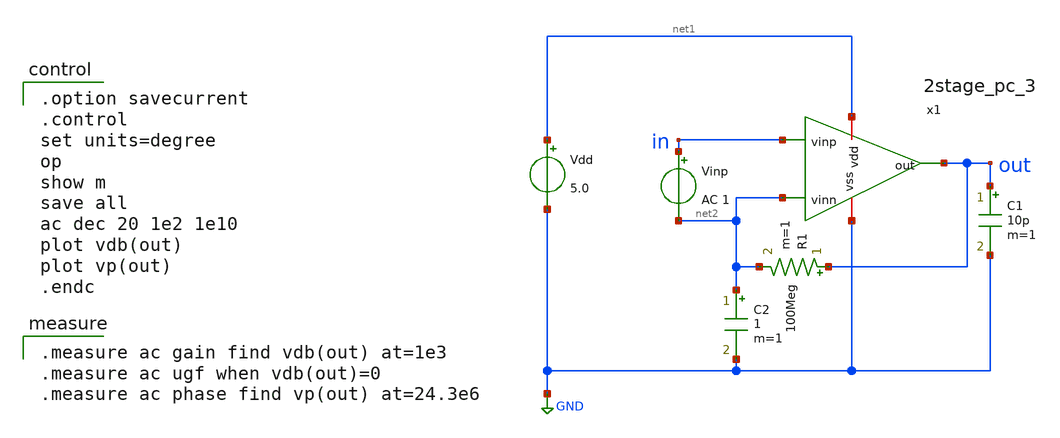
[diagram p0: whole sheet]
** sch_path: member_project/GroupWork/Team_Ando/ugeugeHigh/opamp_cs_ac.sch
**.subckt opamp_cs_ac
Vdd net1 GND 5.0
Vinp in net2 AC 1
C1 out GND 10p m=1
R1 out net2 100Meg m=1
C2 net2 GND 1 m=1
x1 net1 in out net2 GND 2stage_pc_3
**** begin user architecture code

.option savecurrent
.control
set units=degree
op
show m
save all
ac dec 20 1e2 1e10
plot vdb(out)
plot vp(out)
.endc


.measure ac gain find vdb(out) at=1e3
.measure ac ugf when vdb(out)=0
.measure ac phase find vp(out) at=24.3e6

 .include $::LIB/mos.lib
.include $::LIB/passive.lib
.include $::LIB/diode.lib
**** end user architecture code
**.ends

* expanding   symbol:  ishi/2stage_pc_3.sym # of pins=5
** sym_path: member_project/GroupWork/Team_Ando/ugeugeHigh/2stage_pc_3.sym
** sch_path: member_project/GroupWork/Team_Ando/ugeugeHigh/2stage_pc_3.sch
.subckt 2stage_pc_3 vdd vinp out vinn vss
*.ipin vinp
*.ipin vinn
*.opin out
*.iopin vdd
*.iopin vss
M2 net5 net2 net4 vss nmos L=2u W=40u m=1
M6 net2 net3 vdd vdd pmos L=2.5u W=10u m=1
M1 net2 net2 net1 vss nmos L=2u W=10u m=1
M7 net1 net1 vss vss nmos L=2u W=10u m=1
C1 out net5 poly_cap W=18 L=18
M3 net3 net3 vdd vdd pmos L=2.5u W=10u m=1
x1 vdd net3 vinn vinp net4 vss diffwl500-4
x2 vdd net3 out net4 vss source_g
M4 net3 net6 vss vss nmos L=2u W=5u m=1
M5 net6 net6 vss vss nmos L=2u W=5u m=1
M8 net6 net7 vdd vdd pmos L=2.5u W=10u m=1
x3 vdd net8 vss net7 VthRef
.ends


* expanding   symbol:  ishi/diffwl500-4.sym # of pins=6
** sym_path: member_project/GroupWork/Team_Ando/ugeugeHigh/diffwl500-4.sym
** sch_path: member_project/GroupWork/Team_Ando/ugeugeHigh/diffwl500-4.sch
.subckt diffwl500-4 vdd vb vinn vinp out VSS
*.ipin vinn
*.ipin vinp
*.iopin VSS
*.iopin vdd
*.ipin vb
*.opin out
M5 net1 vb vdd vdd pmos L=2u W=40u m=1
M3 net2 net2 VSS VSS nmos L=2u W=10u m=1
M1 net2 vinn net1 net1 pmos L=2u W=200u m=1
M2 out vinp net1 net1 pmos L=2u W=200u m=1
M4 out net2 VSS VSS nmos L=2u W=10u m=1
.ends


* expanding   symbol:  ishi/source_g.sym # of pins=5
** sym_path: member_project/GroupWork/Team_Ando/ugeugeHigh/source_g.sym
** sch_path: member_project/GroupWork/Team_Ando/ugeugeHigh/source_g.sch
.subckt source_g vdd vb out vin VSS
*.iopin vdd
*.opin out
*.ipin vb
*.ipin vin
*.iopin VSS
M2 out vin VSS VSS nmos L=2u W=200u m=1
M1 out vb vdd vdd pmos L=2u W=400u m=1
.ends


* expanding   symbol:  ishi/VthRef.sym # of pins=4
** sym_path: member_project/GroupWork/Team_Ando/YuMaehashi/sch/VthRef.sym
** sch_path: member_project/GroupWork/Team_Ando/YuMaehashi/sch/VthRef.sch
.subckt VthRef VDD VGNOUT VSS VGPOUT
*.iopin VDD
*.iopin VSS
*.opin VGNOUT
*.opin VGPOUT
R1 VSS VGNOUT HR_poly W=4 L=24
M1 netA VGNOUT VSS VSS nmos L=4u W=2u m=2
M2 VGPOUT netA VGNOUT VSS nmos L=2u W=10u m=8
M3 netA VGPOUT VDD VDD pmos L=2.5u W=10u m=10
M4 VGPOUT VGPOUT VDD VDD pmos L=2.5u W=10u m=10
M5 netB netB VSS VSS nmos L=10u W=2u m=1
M6 VDD netB netA VSS nmos L=4u W=2u m=2
M7 net1 VSS VDD VDD pmos L=10u W=2u m=1
M8 netB netB net1 VDD pmos L=10u W=2u m=1
R3 VSS VSS HR_poly W=44 L=24
M9 VSS VSS VSS VSS nmos L=2u W=2u m=1
M10 VSS VSS VGNOUT VSS nmos L=2u W=10u m=2
M11 VDD VDD VDD VDD pmos L=2.5u W=10u m=2
.ends

.GLOBAL GND
.end
